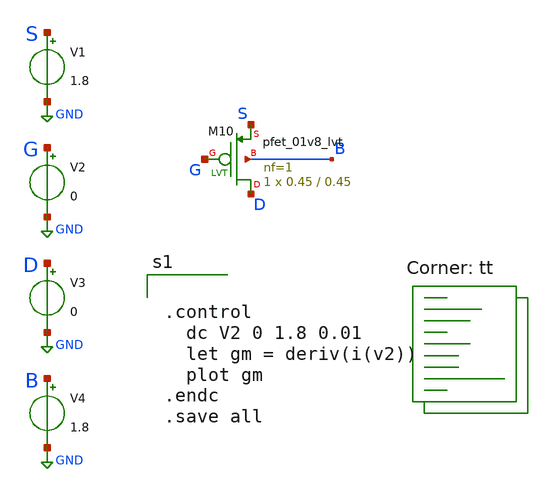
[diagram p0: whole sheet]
** sch_path: designs/tb_xin_neuron_v1/parameters.sch
**.subckt parameters
V1 S GND 1.8
V2 G GND 0
V3 D GND 0
V4 B GND 1.8
XM10 D G S B sky130_fd_pr__pfet_01v8_lvt L=0.45 W=0.45 nf=1 ad='int((1 + 1)/2) * 0.45 / 1 * 0.29' as='int((1 + 2)/2) * 0.45 / 1 * 0.29'
+ pd='2*int((1 + 1)/2) * (0.45 / 1 + 0.29)' ps='2*int((1 + 2)/2) * (0.45 / 1 + 0.29)' nrd='0.29 / 0.45 '
+ nrs='0.29 / 0.45 ' sa=0 sb=0 sd=0 mult=1 m=1
**** begin user architecture code


.control
  dc V2 0 1.8 0.01
  let gm = deriv(i(v2))
  plot gm
.endc
.save all


.lib $::SKYWATER_MODELS/sky130.lib.spice tt
**** end user architecture code
**.ends
.GLOBAL GND
.end
